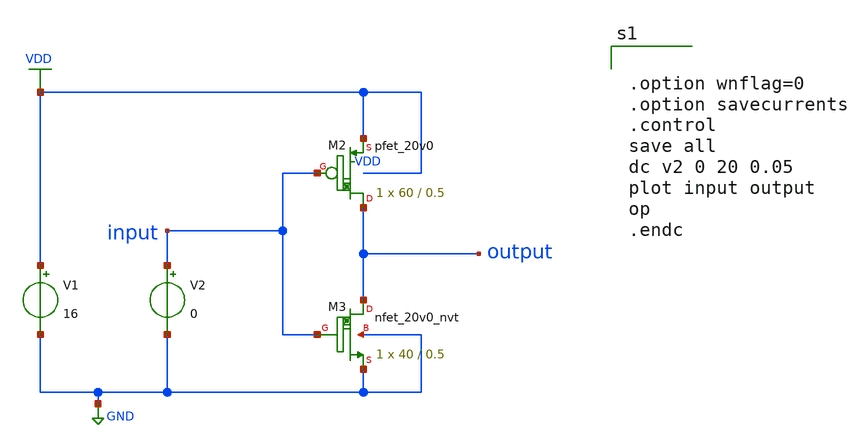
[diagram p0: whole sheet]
** sch_path: schematics/simple_inverter.sch
**.subckt simple_inverter
V1 VDD GND 16
V2 input GND 0
XM2 output input VDD VDD sky130_fd_pr__pfet_20v0 L=0.5 W=60 m=1
XM3 output input GND GND sky130_fd_pr__nfet_20v0_nvt W=40 L=0.5 m=1
**** begin user architecture code
 .lib $::SKYWATER_MODELS/sky130.lib.spice tt
.param mc_mmm_cwitch=0
.param mc_pr_switch=1



.option wnflag=0
.option savecurrents
.control
save all
dc v2 0 20 0.05
plot input output
op
.endc


**** end user architecture code
**.ends
.GLOBAL GND
.GLOBAL VDD
.end
